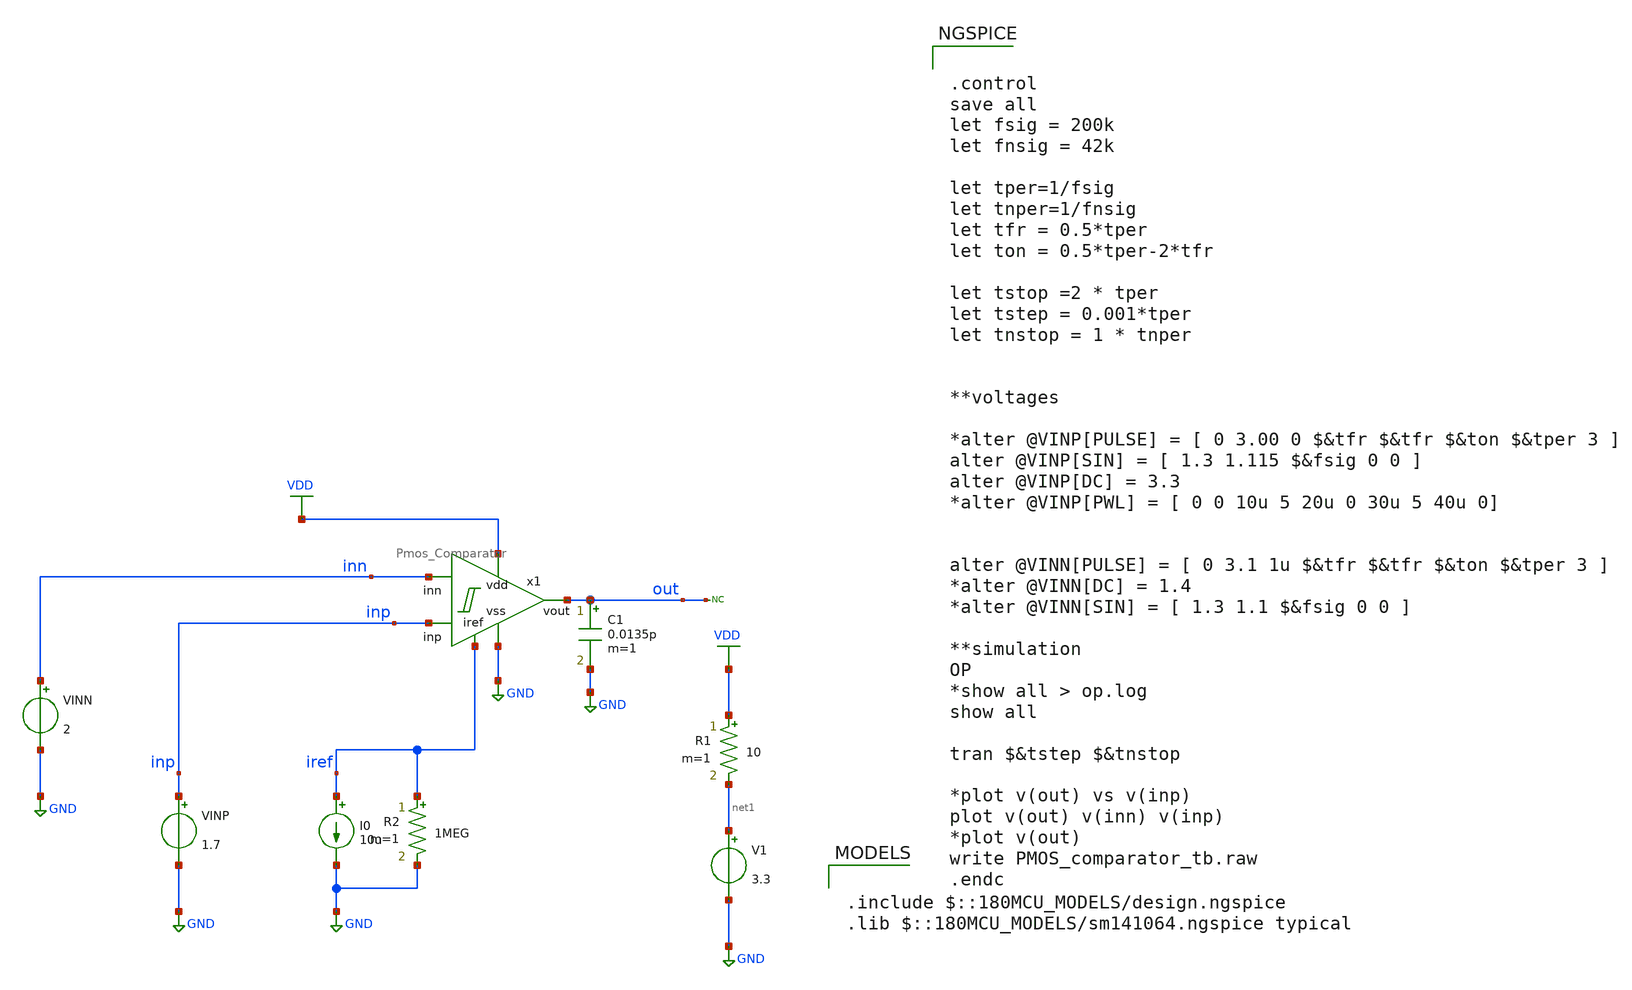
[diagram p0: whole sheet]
** sch_path: designs/libs/tb_analog/Comparator/PMOS_comparator_op_tb.sch
**.subckt PMOS_comparator_op_tb
I0 iref GND 10u
V1 net1 GND 3.3
VINP inp GND 1.7
C1 out GND 0.0135p m=1
* noconn out
VINN inn GND 2
x1 VDD out inp GND inn iref Pmos_Comparator
R1 VDD net1 10 m=1
R2 iref GND 1MEG m=1
**** begin user architecture code


.control
save all
let fsig = 200k
let fnsig = 42k

let tper=1/fsig
let tnper=1/fnsig
let tfr = 0.5*tper
let ton = 0.5*tper-2*tfr

let tstop =2 * tper
let tstep = 0.001*tper
let tnstop = 1 * tnper


**voltages

*alter @VINP[PULSE] = [ 0 3.00 0 $&tfr $&tfr $&ton $&tper 3 ]
alter @VINP[SIN] = [ 1.3 1.115 $&fsig 0 0 ]
alter @VINP[DC] = 3.3
*alter @VINP[PWL] = [ 0 0 10u 5 20u 0 30u 5 40u 0]


alter @VINN[PULSE] = [ 0 3.1 1u $&tfr $&tfr $&ton $&tper 3 ]
*alter @VINN[DC] = 1.4
*alter @VINN[SIN] = [ 1.3 1.1 $&fsig 0 0 ]

**simulation
OP
*show all > op.log
show all

tran $&tstep $&tnstop

*plot v(out) vs v(inp)
plot v(out) v(inn) v(inp)
*plot v(out)
write PMOS_comparator_tb.raw
.endc



.include $::180MCU_MODELS/design.ngspice
.lib $::180MCU_MODELS/sm141064.ngspice typical

**** end user architecture code
**.ends
.GLOBAL GND
.GLOBAL VDD
.end
